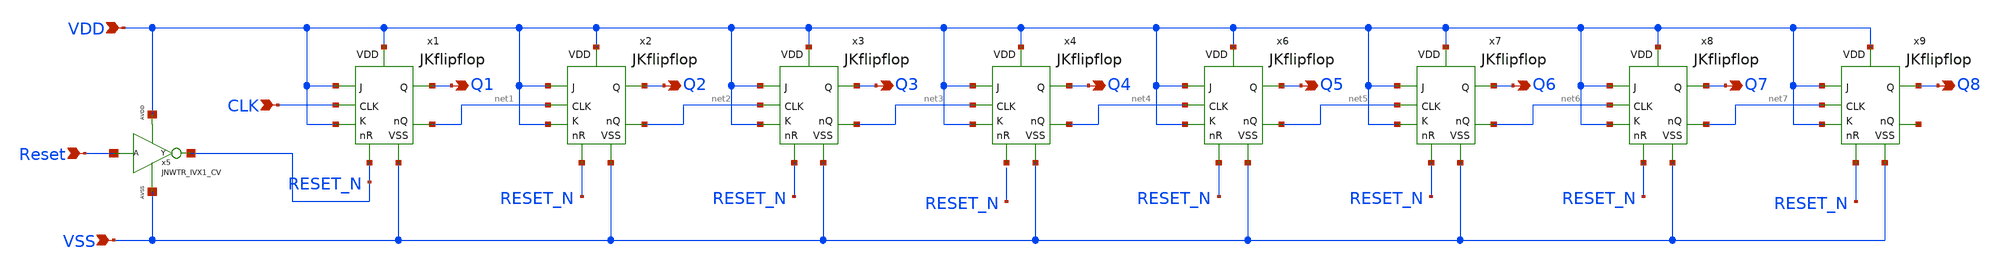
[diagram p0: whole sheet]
** sch_path: design/JNW_GR05_SKY130A/asynCounter_8bit.sch
**.subckt asynCounter_8bit VDD Q1 VSS CLK Q2 Q3 Q4 Reset Q5 Q6 Q7 Q8
*.ipin VDD
*.opin Q1
*.ipin VSS
*.ipin CLK
*.opin Q2
*.opin Q3
*.opin Q4
*.ipin Reset
*.opin Q5
*.opin Q6
*.opin Q7
*.opin Q8
x1 VDD VDD Q1 CLK net1 VDD VSS RESET_N JKflipflop
x2 VDD VDD Q2 net1 net2 VDD VSS RESET_N JKflipflop
x3 VDD VDD Q3 net2 net3 VDD VSS RESET_N JKflipflop
x4 VDD VDD Q4 net3 net4 VDD VSS net8 JKflipflop
x5 Reset RESET_N VDD VSS JNWTR_IVX1_CV
x6 VDD VDD Q5 net4 net5 VDD VSS RESET_N JKflipflop
x7 VDD VDD Q6 net5 net6 VDD VSS RESET_N JKflipflop
x8 VDD VDD Q7 net6 net7 VDD VSS RESET_N JKflipflop
x9 VDD VDD Q8 net7 net9 VDD VSS RESET_N JKflipflop
**.ends
.end
